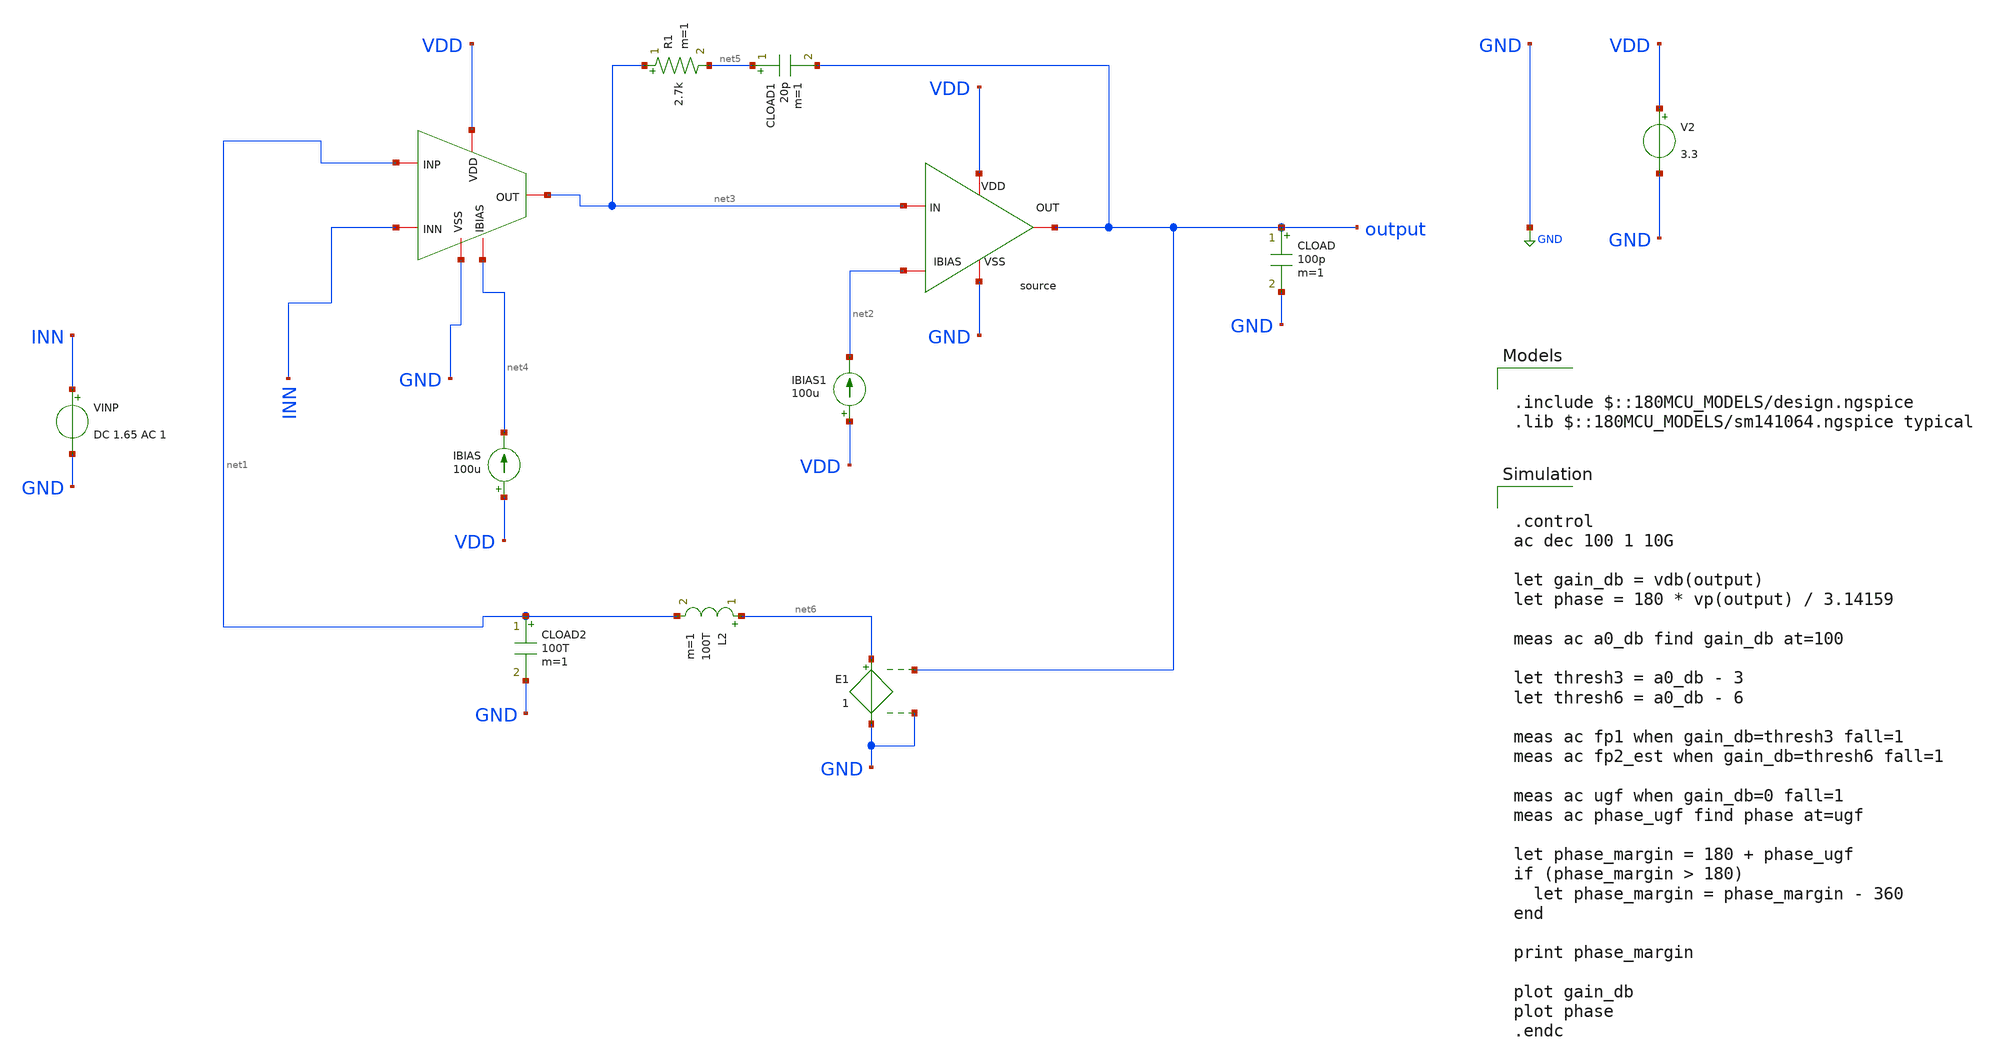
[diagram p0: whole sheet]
** sch_path: designs/libs/core_amps/two_stage_amps/folded_cs_ac_comp_tb.sch
**.subckt folded_cs_ac_comp_tb
x2 VDD net3 net2 output GND cs_schematic
V2 VDD GND 3.3
IBIAS VDD net4 100u
IBIAS1 VDD net2 100u
CLOAD output GND 100p m=1
CLOAD1 net5 output 20p m=1
R1 net3 net5 2.7k m=1
VINP INN GND DC 1.65 AC 1
L2 net6 net1 100T m=1
CLOAD2 net1 GND 100T m=1
E1 net6 GND output GND 1
x1 VDD GND net3 net1 INN net4 ota_folded_cascode
**** begin user architecture code

.include $::180MCU_MODELS/design.ngspice
.lib $::180MCU_MODELS/sm141064.ngspice typical



.control
ac dec 100 1 10G

let gain_db = vdb(output)
let phase = 180 * vp(output) / 3.14159

meas ac a0_db find gain_db at=100

let thresh3 = a0_db - 3
let thresh6 = a0_db - 6

meas ac fp1 when gain_db=thresh3 fall=1
meas ac fp2_est when gain_db=thresh6 fall=1

meas ac ugf when gain_db=0 fall=1
meas ac phase_ugf find phase at=ugf

let phase_margin = 180 + phase_ugf
if (phase_margin > 180)
  let phase_margin = phase_margin - 360
end

print phase_margin

plot gain_db
plot phase
.endc



**** end user architecture code
**.ends
.GLOBAL GND
.end
